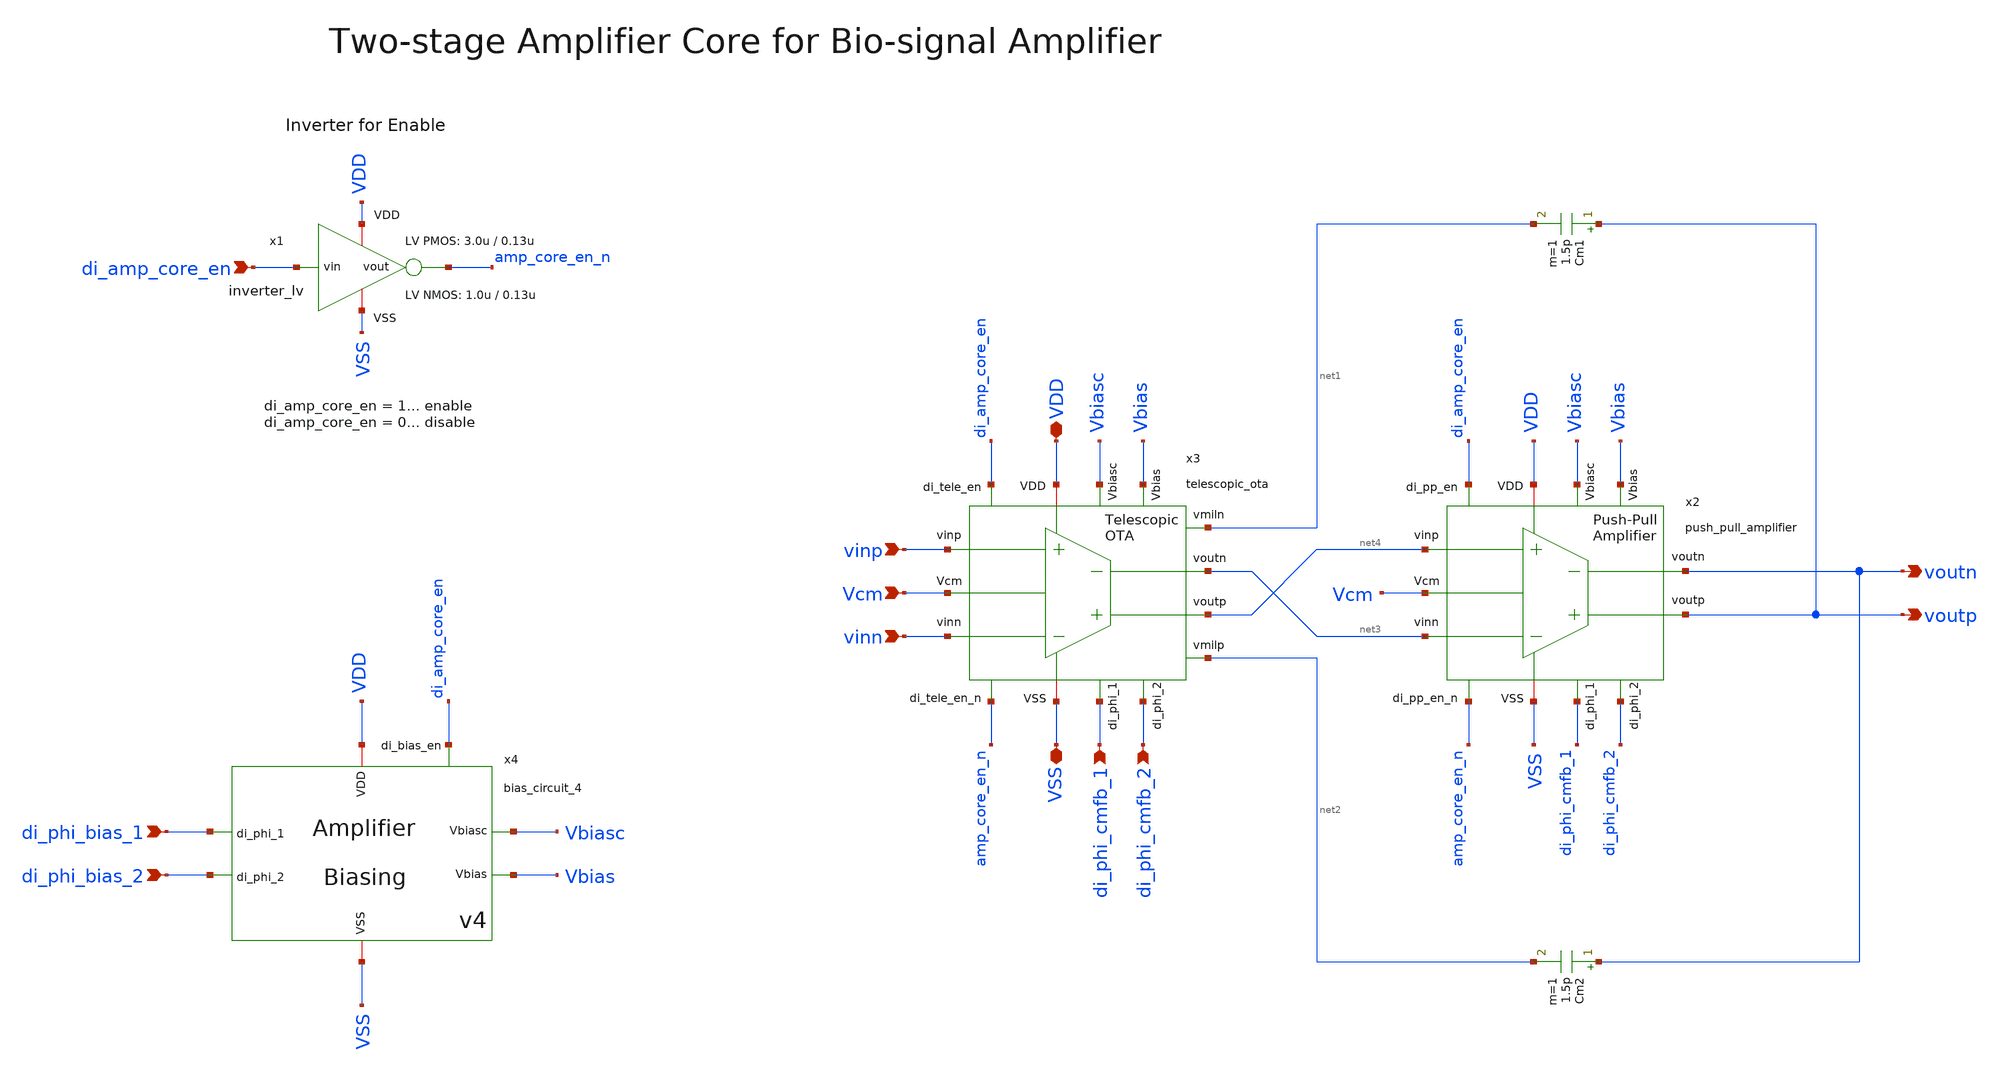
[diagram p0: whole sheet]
** sch_path: SG13G2_ATBS-ADC-main/xschem/bio_amplifier/amplifier_core/amplifier_core.sch
**.subckt amplifier_core di_phi_cmfb_1 di_phi_cmfb_2 di_phi_bias_1 di_phi_bias_2 VDD di_amp_core_en
*+ vinp vinn voutp voutn Vcm VSS
*.ipin di_phi_cmfb_1
*.ipin di_phi_cmfb_2
*.ipin di_phi_bias_1
*.ipin di_phi_bias_2
*.iopin VDD
*.ipin di_amp_core_en
*.ipin vinp
*.ipin vinn
*.opin voutp
*.opin voutn
*.ipin Vcm
*.iopin VSS
x1 VDD di_amp_core_en amp_core_en_n VSS inverter_lv W_P=3.0u L_P=0.13u W_N=1.0u L_N=0.13u
x2 di_phi_cmfb_1 di_phi_cmfb_2 Vcm VDD voutp voutn net3 net4 VSS di_amp_core_en amp_core_en_n Vbiasc
+ Vbias push_pull_amplifier
x3 di_phi_cmfb_1 di_phi_cmfb_2 VDD vinn vinp VSS Vcm di_amp_core_en amp_core_en_n Vbiasc Vbias net1
+ net2 net4 net3 telescopic_ota
Cm1 voutp net1 1.5p m=1
Cm2 voutn net2 1.5p m=1
x4 di_phi_bias_2 di_phi_bias_1 VDD VSS Vbiasc Vbias di_amp_core_en bias_circuit_4
**.ends
.end
